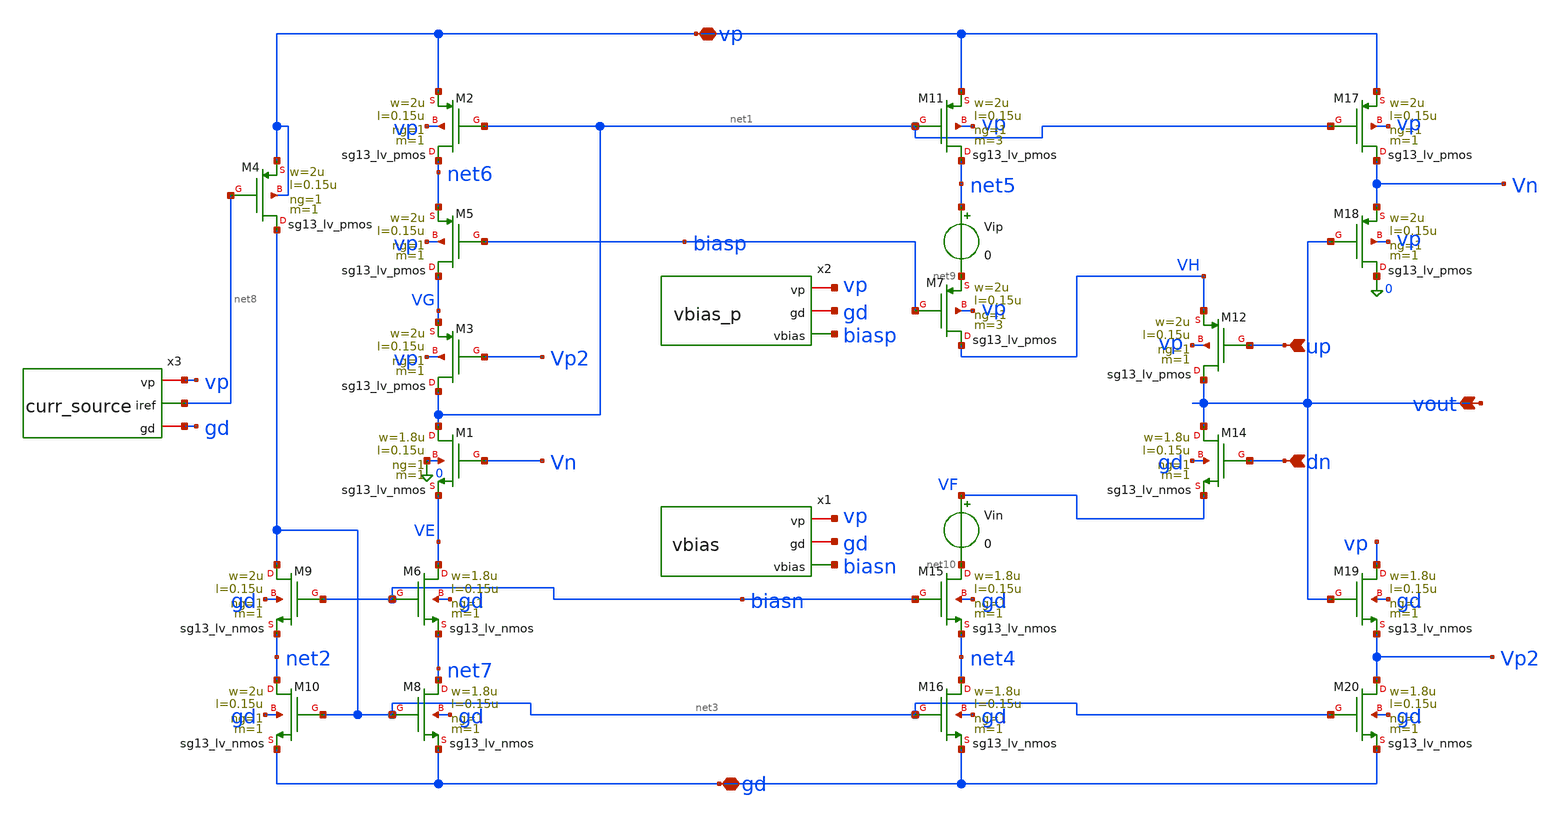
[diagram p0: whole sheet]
** sch_path: PLL0663-main/schematic/xschem/charge_pump/old_sch/cp_v1_no_mirror.sch
**.subckt cp_v1_no_mirror up dn vp gd vout
*.ipin up
*.ipin dn
*.iopin vp
*.iopin gd
*.opin vout
XM7 VH biasp net9 vp sg13_lv_pmos w=2u l=0.15u ng=1 m=3 mm_ok=1
XM12 vout up VH vp sg13_lv_pmos w=2u l=0.15u ng=1 m=1 mm_ok=1
XM14 vout dn VF gd sg13_lv_nmos w=1.8u l=0.15u ng=1 m=1 mm_ok=1
XM15 net10 biasn net4 gd sg13_lv_nmos w=1.8u l=0.15u ng=1 m=1 mm_ok=1
XM16 net4 net3 gd gd sg13_lv_nmos w=1.8u l=0.15u ng=1 m=1 mm_ok=1
XM17 Vn net1 vp vp sg13_lv_pmos w=2u l=0.15u ng=1 m=1 mm_ok=1
XM18 0 vout Vn vp sg13_lv_pmos w=2u l=0.15u ng=1 m=1 mm_ok=1
XM19 vp vout Vp2 gd sg13_lv_nmos w=1.8u l=0.15u ng=1 m=1 mm_ok=1
XM20 Vp2 net3 gd gd sg13_lv_nmos w=1.8u l=0.15u ng=1 m=1 mm_ok=1
XM1 net1 Vn VE 0 sg13_lv_nmos w=1.8u l=0.15u ng=1 m=1 mm_ok=1
XM2 net6 net1 vp vp sg13_lv_pmos w=2u l=0.15u ng=1 m=1 mm_ok=1
XM5 VG biasp net6 vp sg13_lv_pmos w=2u l=0.15u ng=1 m=1 mm_ok=1
XM3 net1 Vp2 VG vp sg13_lv_pmos w=2u l=0.15u ng=1 m=1 mm_ok=1
XM6 VE biasn net7 gd sg13_lv_nmos w=1.8u l=0.15u ng=1 m=1 mm_ok=1
XM8 net7 net3 gd gd sg13_lv_nmos w=1.8u l=0.15u ng=1 m=1 mm_ok=1
XM9 net3 biasn net2 gd sg13_lv_nmos w=2u l=0.15u ng=1 m=1 mm_ok=1
XM10 net2 net3 gd gd sg13_lv_nmos w=2u l=0.15u ng=1 m=1 mm_ok=1
Vip net5 net9 0
Vin VF net10 0
x1 vp gd biasn vbias
x2 vp gd biasp vbias_p
XM11 net5 net1 vp vp sg13_lv_pmos w=2u l=0.15u ng=1 m=3 mm_ok=1
x3 vp net8 gd curr_source
XM4 net3 net8 vp vp sg13_lv_pmos w=2u l=0.15u ng=1 m=1 mm_ok=1
**.ends

* expanding   symbol:  /foss/designs/CHIP-PLL/charge_pump/vbias.sym # of pins=3
** sym_path: schematics/charge_pump/vbias.sym
** sch_path: schematics/charge_pump/vbias.sch
.subckt vbias vp gd vbias
*.opin vbias
*.iopin gd
*.iopin vp
XM5 net1 iref vp vp sg13_lv_pmos w=1.2u l=0.6u ng=1 m=1 mm_ok=1
XM6 vbias net1 net2 gd sg13_lv_nmos w=3.6u l=0.6u ng=1 m=1 mm_ok=1
XM2 net2 net2 gd gd sg13_lv_nmos w=1.2u l=0.6u ng=1 m=1 mm_ok=1
XM3 gd gd gd gd sg13_lv_nmos w=1.86u l=0.6u ng=1 m=1 mm_ok=1
XM7 vp vp vp vp sg13_lv_pmos w=1.375u l=0.6u ng=1 m=1 mm_ok=1
XR1 net1 vbias gd rppd w=1e-6 l=1.7e-6 m=1 b=0 mm_ok=1
x1 vp iref gd curr_source
.ends


* expanding   symbol:  /foss/designs/CHIP-PLL/charge_pump/vbias_p.sym # of pins=3
** sym_path: charge_pump/vbias_p.sym
** sch_path: charge_pump/vbias_p.sch
.subckt vbias_p vp gd vbias
*.iopin vp
*.iopin gd
*.opin vbias
XM16 net2 net2 0 gd sg13_lv_nmos w=1.6u l=0.6u ng=1 m=1 mm_ok=1
XM1 vbias net1 net2 gd sg13_lv_nmos w=1.6u l=0.6u ng=1 m=1 mm_ok=1
R1 net1 vbias 500 m=1
XM5 iref iref vp vp sg13_lv_pmos w=1.4u l=0.6u ng=1 m=1 mm_ok=1
XM6 net3 iref vp vp sg13_lv_pmos w=1u l=0.6u ng=1 m=1 mm_ok=1
XM7 iref net3 net4 gd sg13_lv_nmos w=1u l=0.6u ng=1 m=1 mm_ok=1
XM8 net3 net3 gd gd sg13_lv_nmos w=1.4u l=0.6u ng=1 m=1 mm_ok=1
R3 net4 gd 500 m=1
XM10 net1 iref vp vp sg13_lv_pmos w=1.6u l=0.6u ng=1 m=1 mm_ok=1
.ends


* expanding   symbol:  /foss/designs/CHIP-PLL/charge_pump/curr_source.sym # of pins=3
** sym_path: charge_pump/curr_source.sym
** sch_path: charge_pump/curr_source.sch
.subckt curr_source vp iref gd
*.iopin vp
*.iopin gd
*.opin iref
XM4 iref iref vp vp sg13_lv_pmos w=1.4u l=0.6u ng=1 m=1 mm_ok=1
XM5 net2 iref vp vp sg13_lv_pmos w=1.2u l=0.6u ng=1 m=1 mm_ok=1
XM6 net3 net3 gd gd sg13_lv_nmos w=1u l=0.6u ng=1 m=1 mm_ok=1
XM3 net2 net2 gd gd sg13_lv_nmos w=1.4u l=0.6u ng=1 m=1 mm_ok=1
XR2 net1 gd gd rppd w=1e-6 l=1.70e-6 m=1 b=0 mm_ok=1
XM1 iref net2 net1 gd sg13_lv_nmos w=1.2u l=0.6u ng=1 m=1 mm_ok=1
XM2 vp net3 iref gd sg13_lv_nmos w=1u l=0.6u ng=1 m=1 mm_ok=1
XM7 vp vp net3 gd sg13_lv_nmos w=1u l=0.6u ng=1 m=1 mm_ok=1
XM8 gd gd gd gd sg13_lv_nmos w=0.4u l=0.6u ng=1 m=1 mm_ok=1
.ends

.end
